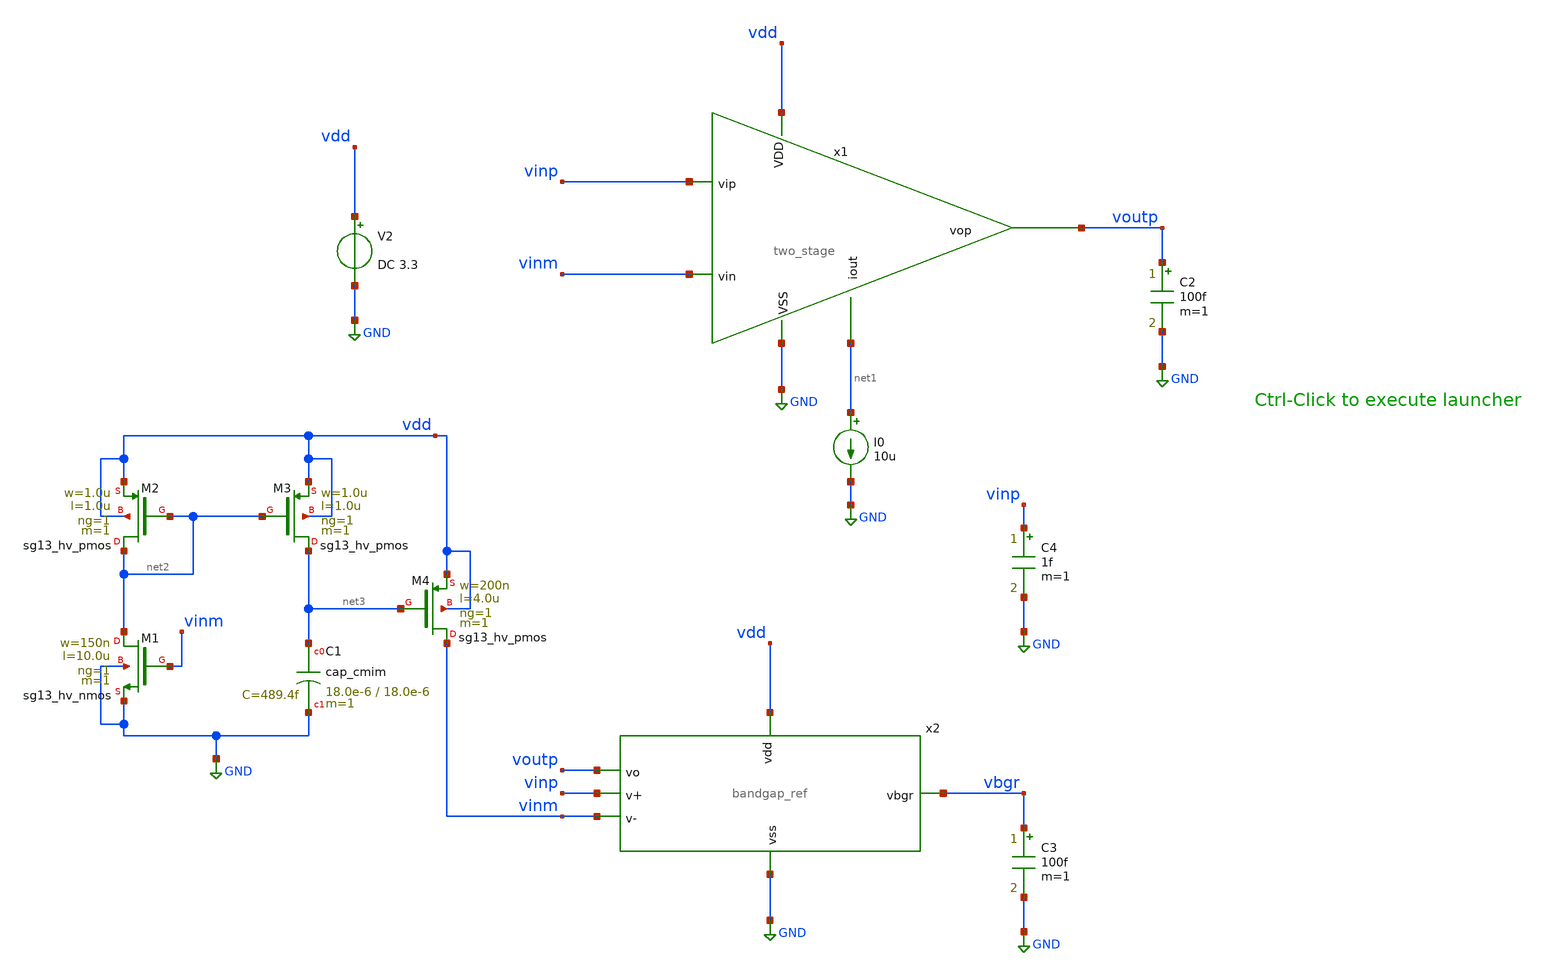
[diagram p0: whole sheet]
** sch_path: testbench/bandgrap_ref_tb.sch
**.subckt bandgrap_ref_tb
V2 vdd GND DC 3.3
x1 vdd voutp vinp vinm GND net1 two_stage
I0 net1 GND 10u
x2 vdd voutp vbgr vinp vinm GND bandgap_ref
XM1 net2 vinm GND GND sg13_hv_nmos w=150n l=10.0u ng=1 m=1 mm_ok=1
XM2 net2 net2 vdd vdd sg13_hv_pmos w=1.0u l=1.0u ng=1 m=1 mm_ok=1
XM3 net3 net2 vdd vdd sg13_hv_pmos w=1.0u l=1.0u ng=1 m=1 mm_ok=1
XC1 net3 GND cap_cmim w=18.0e-6 l=18.0e-6 m=1 mm_ok=1
XM4 vinm net3 vdd vdd sg13_hv_pmos w=200n l=4.0u ng=1 m=1 mm_ok=1
C2 voutp GND 100f m=1
C3 vbgr GND 100f m=1
C4 vinp GND 1f m=1
**** begin user architecture code

.lib cornerMOShv.lib mos_tt
.lib $::SG13G2_MODELS/cornerCAP.lib cap_typ
.lib $::SG13G2_MODELS/cornerRES.lib res_typ



.param temp=27
.control
.include bandgrap_ref_tb.save
.save all
alter V2 dc 3.3
op
dc TEMP -50 100 5
write bgr_temp.raw
.endc

.control
.save all
tran 1m 2
write bgr_tran.raw
.endc


**** end user architecture code
**.ends

* expanding   symbol:  two_stage.sym # of pins=6
** sym_path: schematic/two_stage.sym
** sch_path: schematic/two_stage.sch
.subckt two_stage vdd out v+ v- vss iout
*.opin out
*.ipin iout
*.ipin v-
*.ipin v+
*.ipin vdd
*.ipin vss
XM1 net2 v- net1 vdd sg13_hv_pmos w=23.0u l=5.0u ng=5 m=1 mm_ok=1
XM2 net3 v+ net1 vdd sg13_hv_pmos w=23.0u l=5.0u ng=5 m=1 mm_ok=1
XM5 mirror vb_n net5 vss sg13_hv_nmos w=0.370u l=2.0u ng=1 m=1 mm_ok=1
XM11 net1 iout vdd vdd sg13_hv_pmos w=1.0u l=5.0u ng=1 m=1 mm_ok=1
XM12 iout iout vdd vdd sg13_hv_pmos w=8.5u l=5.0u ng=1 m=1 mm_ok=1
XM3 mirror vb_p net2 vdd sg13_hv_pmos w=1.3u l=1.0u ng=1 m=1 mm_ok=1
XM4 net4 vb_p net3 vdd sg13_hv_pmos w=1.3u l=1.0u ng=1 m=1 mm_ok=1
XM6 net4 vb_n net6 vss sg13_hv_nmos w=0.370u l=2.0u ng=1 m=1 mm_ok=1
XM7 net5 mirror vss vss sg13_hv_nmos w=0.370u l=2.0u ng=1 m=1 mm_ok=1
XM8 net6 mirror vss vss sg13_hv_nmos w=0.370u l=2.0u ng=1 m=1 mm_ok=1
XM9 out net4 vss vss sg13_hv_nmos w=2.35u l=5.00u ng=1 m=1 mm_ok=1
XC1 net4 out cap_cmim w=10.0e-6 l=10.0e-6 m=1 mm_ok=1
XM10 out iout vdd vdd sg13_hv_pmos w=8.5u l=5.0u ng=1 m=1 mm_ok=1
V1 vb_p vss 1.0
V2 vb_n vss 2.0
.ends


* expanding   symbol:  bandgap_ref.sym # of pins=6
** sym_path: schematic/bandgap_ref.sym
** sch_path: schematic/bandgap_ref.sch
.subckt bandgap_ref vdd vo vbgr v+ v- vss
*.ipin vdd
*.ipin vss
*.ipin vo
*.opin vbgr
*.ipin v+
*.ipin v-
XM1 net1 net1 vss vss sg13_hv_nmos w=7.0u l=5.0u ng=1 m=1 mm_ok=1
XM2 v- v+ vss vss sg13_hv_nmos w=7.0u l=5.0u ng=1 m=1 mm_ok=1
XM3 v- vo vdd vdd sg13_hv_pmos w=15.0u l=5.0u ng=5 m=1 mm_ok=1
XM4 v+ vo vdd vdd sg13_hv_pmos w=15.0u l=5.0u ng=5 m=1 mm_ok=1
XR1 v+ net1 sub! rppd w=0.5e-6 l=200e-6 m=1 b=0 mm_ok=1
XM5 vbgr vo vdd vdd sg13_hv_pmos w=15.0u l=5.0u ng=5 m=1 mm_ok=1
XR3 v+ vss sub! rppd w=0.5e-6 l=200e-6 m=1 b=0 mm_ok=1
XR4 vbgr vss sub! rppd w=0.5e-6 l=200e-6 m=1 b=0 mm_ok=1
XC1 vbgr vss cap_cmim w=7.0e-6 l=7.0e-6 m=1 mm_ok=1
.ends

.GLOBAL GND
.end
